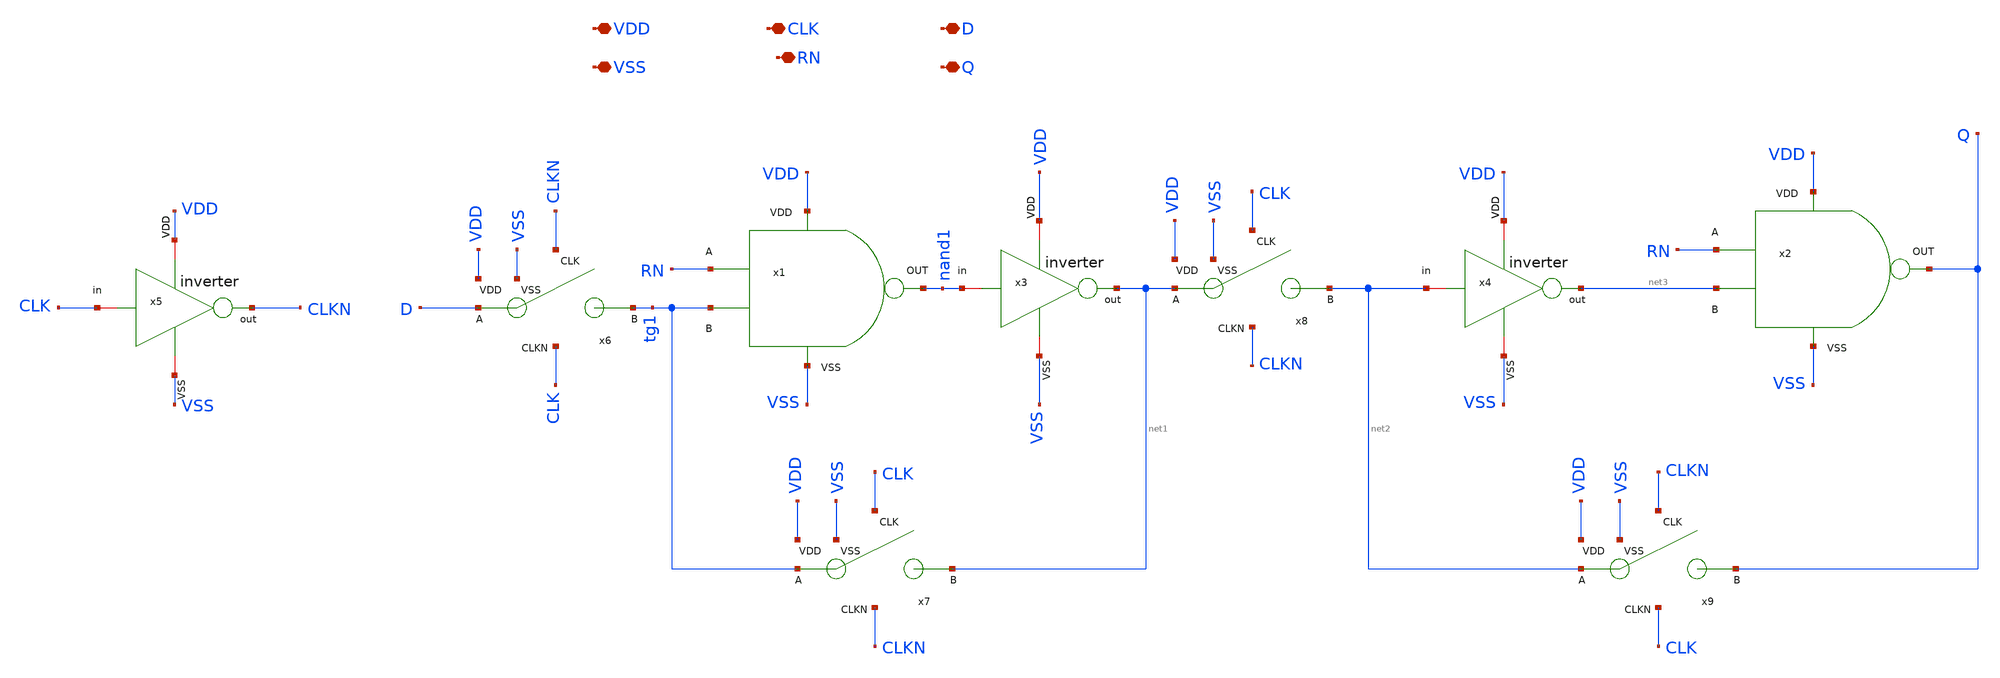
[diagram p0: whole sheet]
** sch_path: designs/sar_adc/digital/flip_flop/xschem/FF_D.sch
**.subckt FF_D VDD VSS CLK D RN Q
*.iopin VDD
*.iopin VSS
*.iopin CLK
*.iopin D
*.iopin RN
*.iopin Q
x1 VDD VSS RN tg1 nand1 NAND
x2 VDD VSS RN net3 Q NAND
x3 VDD nand1 net1 VSS inverter
x4 VDD net2 net3 VSS inverter
x5 VDD CLK CLKN VSS inverter
x6 CLKN D VDD tg1 CLK VSS TG
x7 CLK tg1 VDD net1 CLKN VSS TG
x8 CLK net1 VDD net2 CLKN VSS TG
x9 CLKN net2 VDD Q CLK VSS TG
**.ends

* expanding   symbol:  sar_adc/digital/NAND/xschem/NAND.sym # of pins=5
** sym_path: designs/sar_adc/digital/NAND/xschem/NAND.sym
** sch_path: designs/sar_adc/digital/NAND/xschem/NAND.sch
.subckt NAND VDD VSS A B out
*.iopin VDD
*.iopin A
*.iopin B
*.iopin out
*.iopin VSS
xINVA VDD net1 net2 VSS inverter
xINVB[2] VDD net2 out VSS inverter
xINVB[1] VDD net2 out VSS inverter
xINVB[0] VDD net2 out VSS inverter
XM2 net1 A VDD VDD pfet_03v3 L=0.28u W=0.5u nf=1 ad='int((nf+1)/2) * W/nf * 0.18u' as='int((nf+2)/2) * W/nf * 0.18u'
+ pd='2*int((nf+1)/2) * (W/nf + 0.18u)' ps='2*int((nf+2)/2) * (W/nf + 0.18u)' nrd='0.18u / W' nrs='0.18u / W'
+ sa=0 sb=0 sd=0 m=2
XM1 net1 A net3 VSS nfet_03v3 L=0.28u W=0.5u nf=1 ad='int((nf+1)/2) * W/nf * 0.18u' as='int((nf+2)/2) * W/nf * 0.18u'
+ pd='2*int((nf+1)/2) * (W/nf + 0.18u)' ps='2*int((nf+2)/2) * (W/nf + 0.18u)' nrd='0.18u / W' nrs='0.18u / W'
+ sa=0 sb=0 sd=0 m=1
XM3 net1 B VDD VDD pfet_03v3 L=0.28u W=0.5u nf=1 ad='int((nf+1)/2) * W/nf * 0.18u' as='int((nf+2)/2) * W/nf * 0.18u'
+ pd='2*int((nf+1)/2) * (W/nf + 0.18u)' ps='2*int((nf+2)/2) * (W/nf + 0.18u)' nrd='0.18u / W' nrs='0.18u / W'
+ sa=0 sb=0 sd=0 m=2
XM4 net3 B VSS VSS nfet_03v3 L=0.28u W=0.5u nf=1 ad='int((nf+1)/2) * W/nf * 0.18u' as='int((nf+2)/2) * W/nf * 0.18u'
+ pd='2*int((nf+1)/2) * (W/nf + 0.18u)' ps='2*int((nf+2)/2) * (W/nf + 0.18u)' nrd='0.18u / W' nrs='0.18u / W'
+ sa=0 sb=0 sd=0 m=1
.ends


* expanding   symbol:  sar_adc/digital/inverter/xschem/inverter.sym # of pins=6
** sym_path: designs/sar_adc/digital/inverter/xschem/inverter.sym
** sch_path: designs/sar_adc/digital/inverter/xschem/inverter.sch
.subckt inverter VDD in out VSS
*.opin out
*.iopin in
*.iopin VDD
*.iopin VSS
XM1 out in VSS VSS nfet_03v3 L=0.28u W=1u nf=1 ad='int((nf+1)/2) * W/nf * 0.18u' as='int((nf+2)/2) * W/nf * 0.18u'
+ pd='2*int((nf+1)/2) * (W/nf + 0.18u)' ps='2*int((nf+2)/2) * (W/nf + 0.18u)' nrd='0.18u / W' nrs='0.18u / W'
+ sa=0 sb=0 sd=0 m=1
XM2 out in VDD VDD pfet_03v3 L=0.28u W=3u nf=1 ad='int((nf+1)/2) * W/nf * 0.18u' as='int((nf+2)/2) * W/nf * 0.18u'
+ pd='2*int((nf+1)/2) * (W/nf + 0.18u)' ps='2*int((nf+2)/2) * (W/nf + 0.18u)' nrd='0.18u / W' nrs='0.18u / W'
+ sa=0 sb=0 sd=0 m=1
.ends


* expanding   symbol:  sar_adc/digital/TG/xschem/TG.sym # of pins=6
** sym_path: designs/sar_adc/digital/TG/xschem/TG.sym
** sch_path: designs/sar_adc/digital/TG/xschem/TG.sch
.subckt TG CLK A VDD B CLKN VSS
*.iopin VDD
*.iopin VSS
*.ipin CLK
*.ipin CLKN
*.iopin A
*.iopin B
XM1 A CLK B VSS nfet_03v3 L=0.28u W=0.22u nf=1 ad='int((nf+1)/2) * W/nf * 0.18u' as='int((nf+2)/2) * W/nf * 0.18u'
+ pd='2*int((nf+1)/2) * (W/nf + 0.18u)' ps='2*int((nf+2)/2) * (W/nf + 0.18u)' nrd='0.18u / W' nrs='0.18u / W'
+ sa=0 sb=0 sd=0 m=1
XM2 A CLKN B VDD pfet_03v3 L=0.28u W=0.22u nf=1 ad='int((nf+1)/2) * W/nf * 0.18u' as='int((nf+2)/2) * W/nf * 0.18u'
+ pd='2*int((nf+1)/2) * (W/nf + 0.18u)' ps='2*int((nf+2)/2) * (W/nf + 0.18u)' nrd='0.18u / W' nrs='0.18u / W'
+ sa=0 sb=0 sd=0 m=1
.ends

.end
